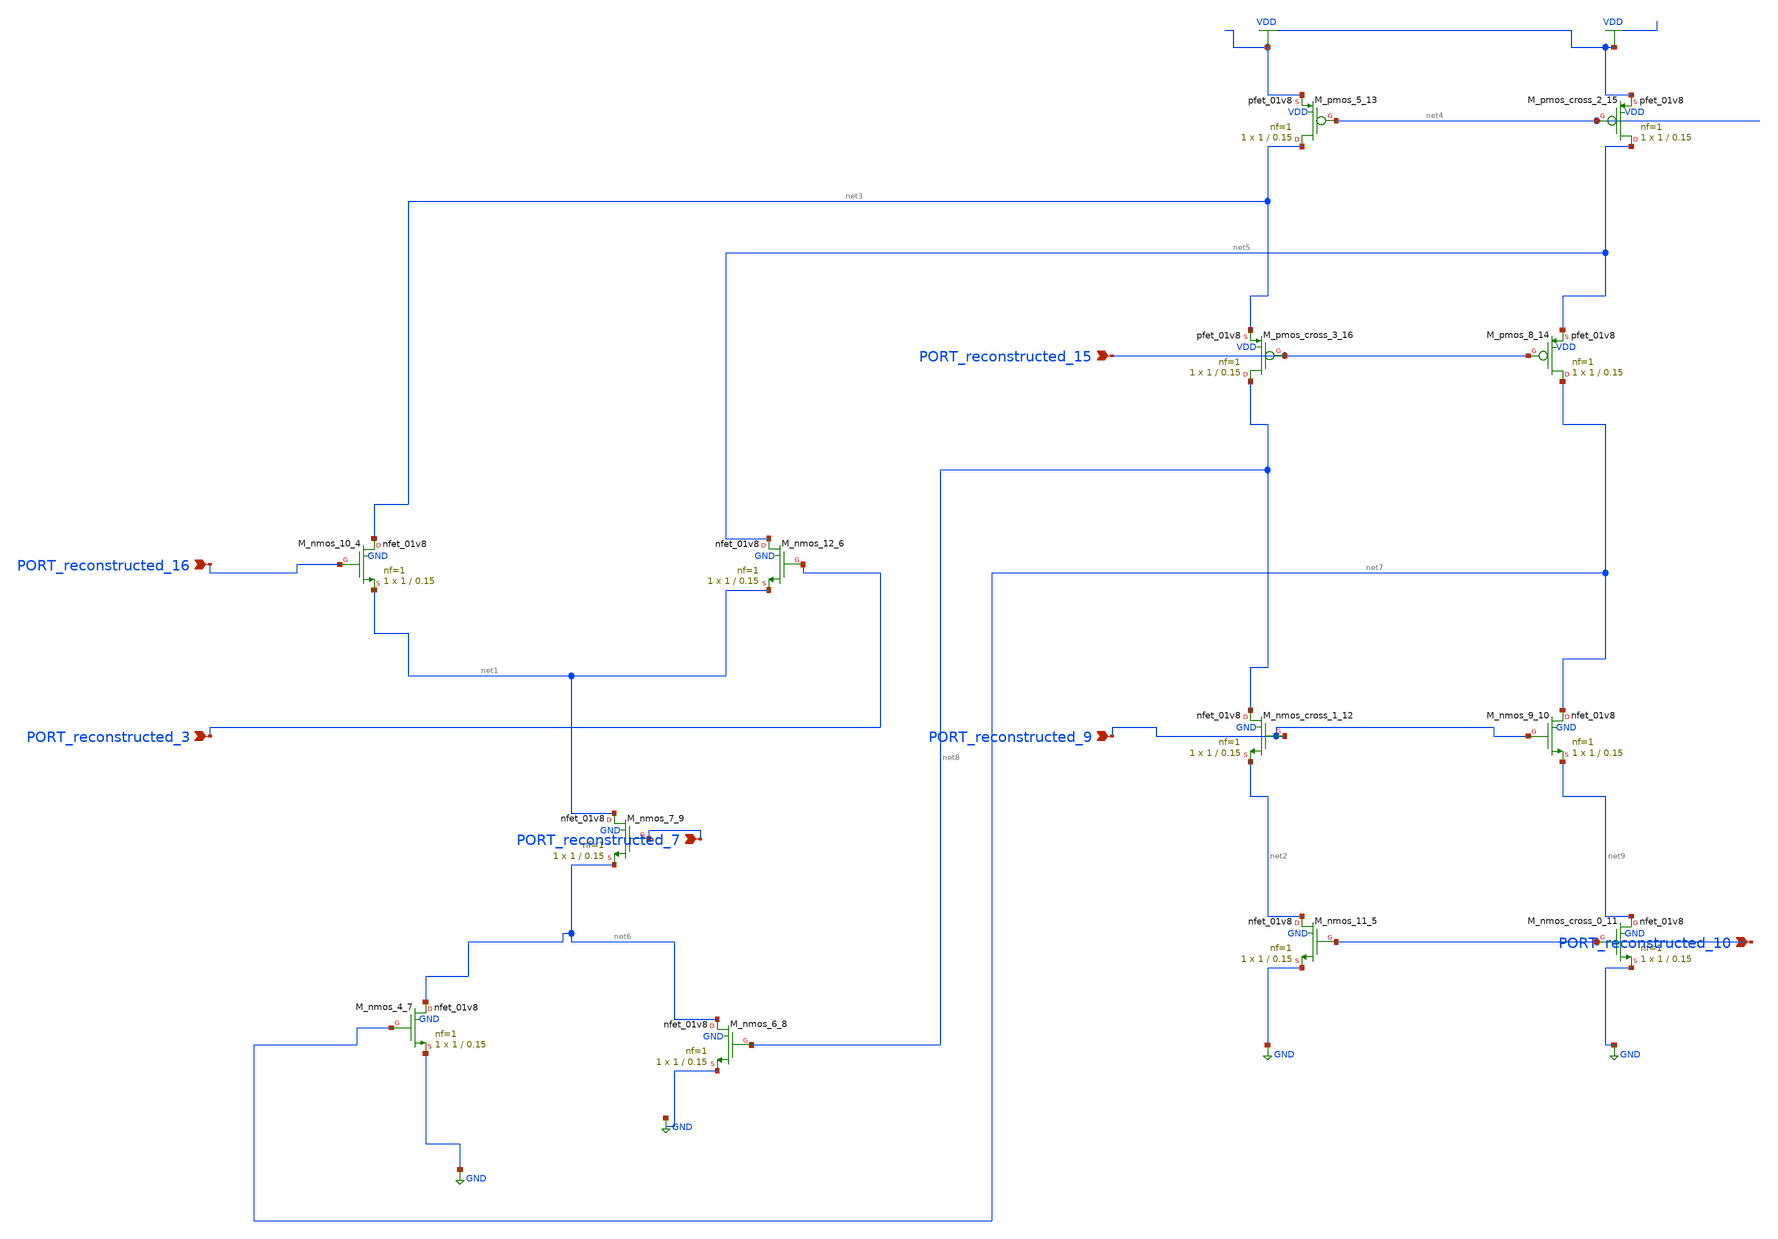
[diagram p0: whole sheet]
** sch_path: schematics/AMSNet/669.sch
**.subckt 669 PORT_reconstructed_16 PORT_reconstructed_7 PORT_reconstructed_3 PORT_reconstructed_10
*+ PORT_reconstructed_9 PORT_reconstructed_15
*.ipin PORT_reconstructed_16
*.ipin PORT_reconstructed_7
*.ipin PORT_reconstructed_3
*.ipin PORT_reconstructed_10
*.ipin PORT_reconstructed_9
*.ipin PORT_reconstructed_15
XM_nmos_10_4 net3 PORT_reconstructed_16 net1 GND sky130_fd_pr__nfet_01v8 L=0.15 W=1 nf=1 ad='int((1 + 1)/2) * 1 / 1 * 0.29'
+ as='int((1 + 2)/2) * 1 / 1 * 0.29' pd='2*int((1 + 1)/2) * (1 / 1 + 0.29)' ps='2*int((1 + 2)/2) * (1 / 1 + 0.29)'
+ nrd='0.29 / 1 ' nrs='0.29 / 1 ' sa=0 sb=0 sd=0 mult=1 m=1
XM_nmos_11_5 net2 PORT_reconstructed_10 GND GND sky130_fd_pr__nfet_01v8 L=0.15 W=1 nf=1 ad='int((1 + 1)/2) * 1 / 1 * 0.29'
+ as='int((1 + 2)/2) * 1 / 1 * 0.29' pd='2*int((1 + 1)/2) * (1 / 1 + 0.29)' ps='2*int((1 + 2)/2) * (1 / 1 + 0.29)'
+ nrd='0.29 / 1 ' nrs='0.29 / 1 ' sa=0 sb=0 sd=0 mult=1 m=1
XM_nmos_12_6 net5 PORT_reconstructed_3 net1 GND sky130_fd_pr__nfet_01v8 L=0.15 W=1 nf=1 ad='int((1 + 1)/2) * 1 / 1 * 0.29'
+ as='int((1 + 2)/2) * 1 / 1 * 0.29' pd='2*int((1 + 1)/2) * (1 / 1 + 0.29)' ps='2*int((1 + 2)/2) * (1 / 1 + 0.29)'
+ nrd='0.29 / 1 ' nrs='0.29 / 1 ' sa=0 sb=0 sd=0 mult=1 m=1
XM_nmos_4_7 net6 net7 GND GND sky130_fd_pr__nfet_01v8 L=0.15 W=1 nf=1 ad='int((1 + 1)/2) * 1 / 1 * 0.29'
+ as='int((1 + 2)/2) * 1 / 1 * 0.29' pd='2*int((1 + 1)/2) * (1 / 1 + 0.29)' ps='2*int((1 + 2)/2) * (1 / 1 + 0.29)'
+ nrd='0.29 / 1 ' nrs='0.29 / 1 ' sa=0 sb=0 sd=0 mult=1 m=1
XM_nmos_6_8 net6 net8 GND GND sky130_fd_pr__nfet_01v8 L=0.15 W=1 nf=1 ad='int((1 + 1)/2) * 1 / 1 * 0.29'
+ as='int((1 + 2)/2) * 1 / 1 * 0.29' pd='2*int((1 + 1)/2) * (1 / 1 + 0.29)' ps='2*int((1 + 2)/2) * (1 / 1 + 0.29)'
+ nrd='0.29 / 1 ' nrs='0.29 / 1 ' sa=0 sb=0 sd=0 mult=1 m=1
XM_nmos_7_9 net1 PORT_reconstructed_7 net6 GND sky130_fd_pr__nfet_01v8 L=0.15 W=1 nf=1 ad='int((1 + 1)/2) * 1 / 1 * 0.29'
+ as='int((1 + 2)/2) * 1 / 1 * 0.29' pd='2*int((1 + 1)/2) * (1 / 1 + 0.29)' ps='2*int((1 + 2)/2) * (1 / 1 + 0.29)'
+ nrd='0.29 / 1 ' nrs='0.29 / 1 ' sa=0 sb=0 sd=0 mult=1 m=1
XM_nmos_9_10 net7 PORT_reconstructed_9 net9 GND sky130_fd_pr__nfet_01v8 L=0.15 W=1 nf=1 ad='int((1 + 1)/2) * 1 / 1 * 0.29'
+ as='int((1 + 2)/2) * 1 / 1 * 0.29' pd='2*int((1 + 1)/2) * (1 / 1 + 0.29)' ps='2*int((1 + 2)/2) * (1 / 1 + 0.29)'
+ nrd='0.29 / 1 ' nrs='0.29 / 1 ' sa=0 sb=0 sd=0 mult=1 m=1
XM_nmos_cross_0_11 net9 PORT_reconstructed_10 GND GND sky130_fd_pr__nfet_01v8 L=0.15 W=1 nf=1 ad='int((1 + 1)/2) * 1 / 1 * 0.29'
+ as='int((1 + 2)/2) * 1 / 1 * 0.29' pd='2*int((1 + 1)/2) * (1 / 1 + 0.29)' ps='2*int((1 + 2)/2) * (1 / 1 + 0.29)'
+ nrd='0.29 / 1 ' nrs='0.29 / 1 ' sa=0 sb=0 sd=0 mult=1 m=1
XM_nmos_cross_1_12 net8 PORT_reconstructed_9 net2 GND sky130_fd_pr__nfet_01v8 L=0.15 W=1 nf=1 ad='int((1 + 1)/2) * 1 / 1 * 0.29'
+ as='int((1 + 2)/2) * 1 / 1 * 0.29' pd='2*int((1 + 1)/2) * (1 / 1 + 0.29)' ps='2*int((1 + 2)/2) * (1 / 1 + 0.29)'
+ nrd='0.29 / 1 ' nrs='0.29 / 1 ' sa=0 sb=0 sd=0 mult=1 m=1
XM_pmos_5_13 net3 net4 VDD VDD sky130_fd_pr__pfet_01v8 L=0.15 W=1 nf=1 ad='int((1 + 1)/2) * 1 / 1 * 0.29'
+ as='int((1 + 2)/2) * 1 / 1 * 0.29' pd='2*int((1 + 1)/2) * (1 / 1 + 0.29)' ps='2*int((1 + 2)/2) * (1 / 1 + 0.29)'
+ nrd='0.29 / 1 ' nrs='0.29 / 1 ' sa=0 sb=0 sd=0 mult=1 m=1
XM_pmos_8_14 net7 PORT_reconstructed_15 net5 VDD sky130_fd_pr__pfet_01v8 L=0.15 W=1 nf=1 ad='int((1 + 1)/2) * 1 / 1 * 0.29'
+ as='int((1 + 2)/2) * 1 / 1 * 0.29' pd='2*int((1 + 1)/2) * (1 / 1 + 0.29)' ps='2*int((1 + 2)/2) * (1 / 1 + 0.29)'
+ nrd='0.29 / 1 ' nrs='0.29 / 1 ' sa=0 sb=0 sd=0 mult=1 m=1
XM_pmos_cross_2_15 net5 net4 VDD VDD sky130_fd_pr__pfet_01v8 L=0.15 W=1 nf=1 ad='int((1 + 1)/2) * 1 / 1 * 0.29'
+ as='int((1 + 2)/2) * 1 / 1 * 0.29' pd='2*int((1 + 1)/2) * (1 / 1 + 0.29)' ps='2*int((1 + 2)/2) * (1 / 1 + 0.29)'
+ nrd='0.29 / 1 ' nrs='0.29 / 1 ' sa=0 sb=0 sd=0 mult=1 m=1
XM_pmos_cross_3_16 net8 PORT_reconstructed_15 net3 VDD sky130_fd_pr__pfet_01v8 L=0.15 W=1 nf=1 ad='int((1 + 1)/2) * 1 / 1 * 0.29'
+ as='int((1 + 2)/2) * 1 / 1 * 0.29' pd='2*int((1 + 1)/2) * (1 / 1 + 0.29)' ps='2*int((1 + 2)/2) * (1 / 1 + 0.29)'
+ nrd='0.29 / 1 ' nrs='0.29 / 1 ' sa=0 sb=0 sd=0 mult=1 m=1
**.ends
.GLOBAL GND
.GLOBAL VDD
.end
